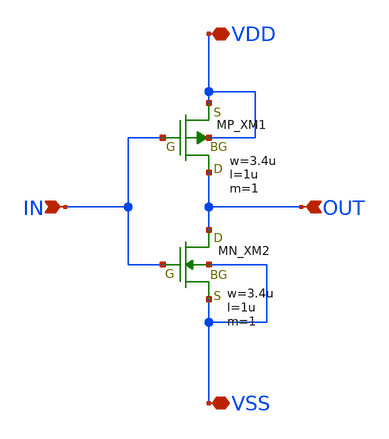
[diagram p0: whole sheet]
** sch_path: member_project/inverter/RISE-A/7158918/inverter.sch
**.subckt inverter OUT IN VDD VSS
*.ipin OUT
*.ipin IN
*.iopin VDD
*.iopin VSS
XXM1 OUT IN VDD VDD PMOS w=3.4u l=1u nrd=0 nrs=0 m=1
XXM2 OUT IN VSS VSS NMOS w=3.4u l=1u nrd=0 nrs=0 m=1
**.ends
.end
